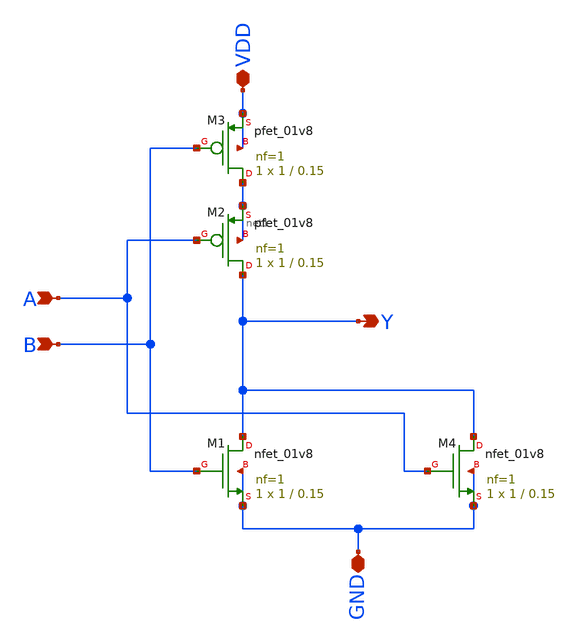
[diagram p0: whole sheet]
** sch_path: designs/nand/xschem/nand.sch
**.subckt nand A B Y GND VDD
*.ipin A
*.ipin B
*.opin Y
*.iopin GND
*.iopin VDD
XM1 Y B GND GND sky130_fd_pr__nfet_01v8 L=0.15 W=1 nf=1 ad='int((1 + 1)/2) * 1 / 1 * 0.29' as='int((1 + 2)/2) * 1 / 1 * 0.29'
+ pd='2*int((1 + 1)/2) * (1 / 1 + 0.29)' ps='2*int((1 + 2)/2) * (1 / 1 + 0.29)' nrd='0.29 / 1 ' nrs='0.29 / 1 '
+ sa=0 sb=0 sd=0 mult=1 m=1
XM2 Y A net1 net1 sky130_fd_pr__pfet_01v8 L=0.15 W=1 nf=1 ad='int((1 + 1)/2) * 1 / 1 * 0.29' as='int((1 + 2)/2) * 1 / 1 * 0.29'
+ pd='2*int((1 + 1)/2) * (1 / 1 + 0.29)' ps='2*int((1 + 2)/2) * (1 / 1 + 0.29)' nrd='0.29 / 1 ' nrs='0.29 / 1 '
+ sa=0 sb=0 sd=0 mult=1 m=1
XM3 net1 B VDD VDD sky130_fd_pr__pfet_01v8 L=0.15 W=1 nf=1 ad='int((1 + 1)/2) * 1 / 1 * 0.29' as='int((1 + 2)/2) * 1 / 1 * 0.29'
+ pd='2*int((1 + 1)/2) * (1 / 1 + 0.29)' ps='2*int((1 + 2)/2) * (1 / 1 + 0.29)' nrd='0.29 / 1 ' nrs='0.29 / 1 '
+ sa=0 sb=0 sd=0 mult=1 m=1
XM4 Y A GND GND sky130_fd_pr__nfet_01v8 L=0.15 W=1 nf=1 ad='int((1 + 1)/2) * 1 / 1 * 0.29' as='int((1 + 2)/2) * 1 / 1 * 0.29'
+ pd='2*int((1 + 1)/2) * (1 / 1 + 0.29)' ps='2*int((1 + 2)/2) * (1 / 1 + 0.29)' nrd='0.29 / 1 ' nrs='0.29 / 1 '
+ sa=0 sb=0 sd=0 mult=1 m=1
**.ends
.end
